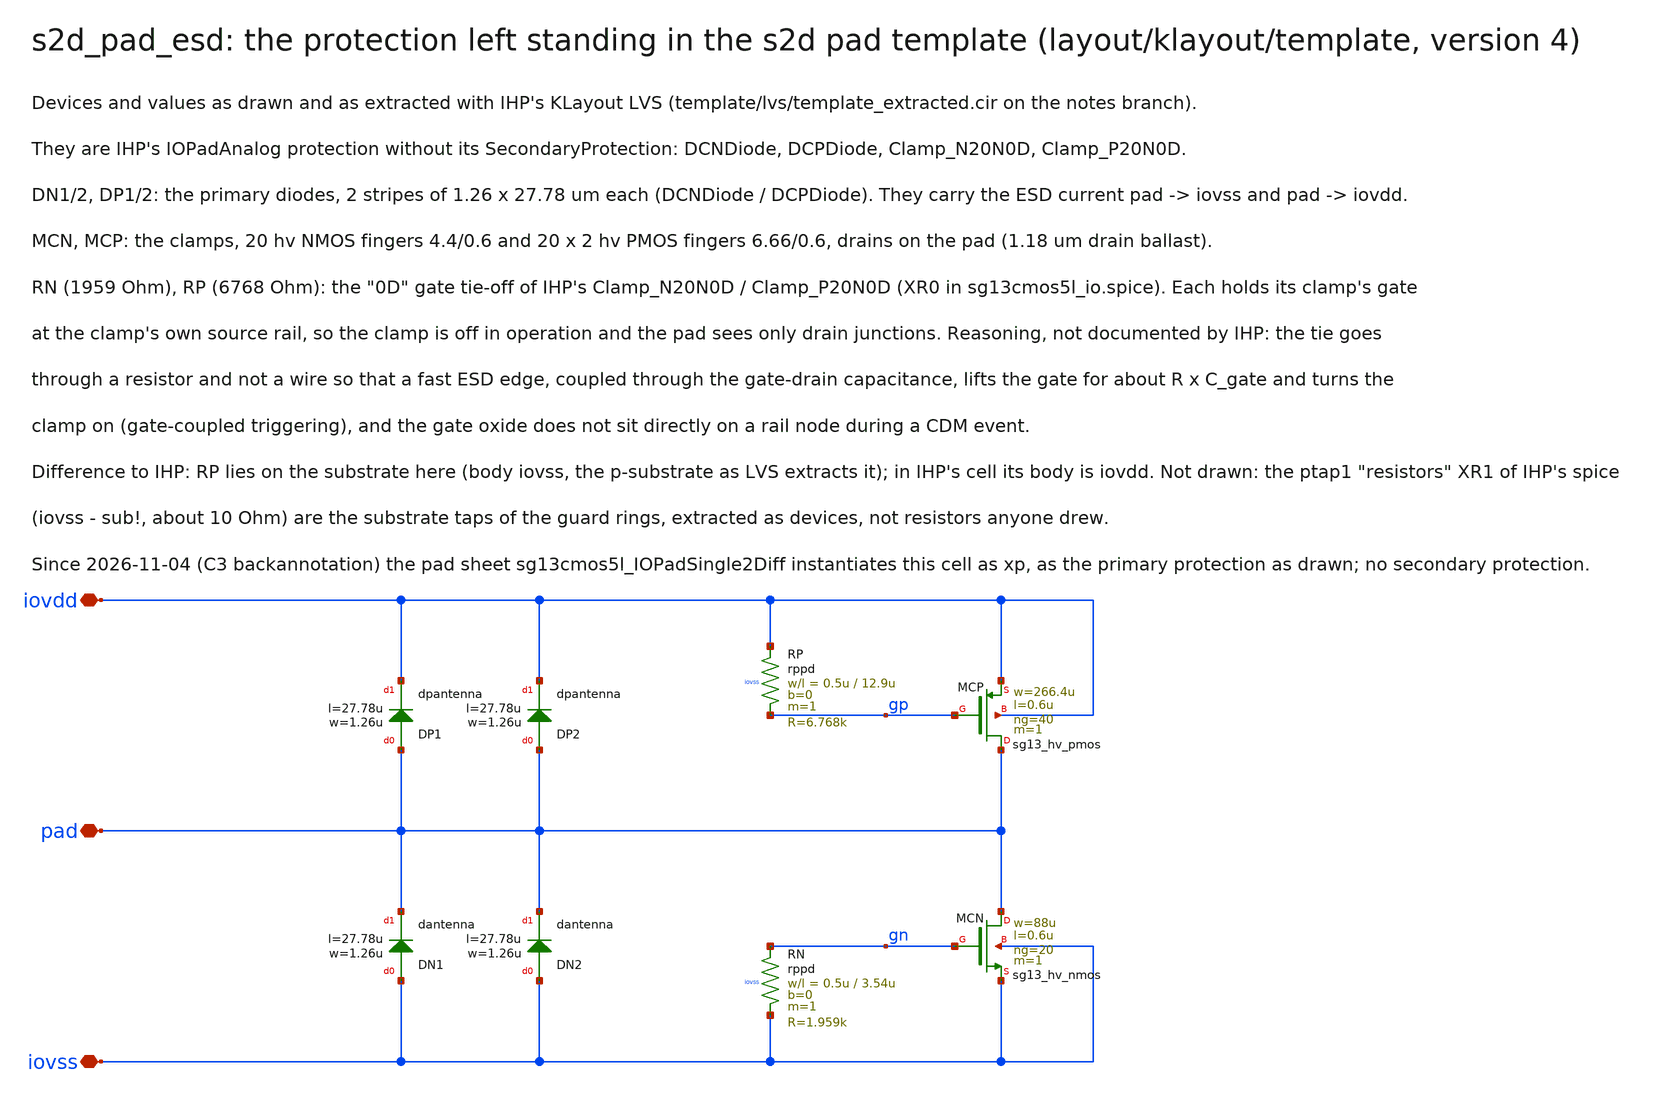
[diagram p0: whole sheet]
** sch_path: macros/sg13cmos5l_IOPadSingle2Diff/schematic/xschem/s2d_pad_esd.sch
**.subckt s2d_pad_esd iovdd iovss pad
*.iopin iovdd
*.iopin iovss
*.iopin pad
XDP1 pad iovdd dpantenna l=27.78u w=1.26u
XDN1 iovss pad dantenna l=27.78u w=1.26u
XDP2 pad iovdd dpantenna l=27.78u w=1.26u
XDN2 iovss pad dantenna l=27.78u w=1.26u
XRP iovdd gp iovss rppd w=0.5u l=12.9u m=1 b=0 mm_ok=1
XMCP pad gp iovdd iovdd sg13_hv_pmos w=266.4u l=0.6u ng=40 m=1 mm_ok=1
XRN gn iovss iovss rppd w=0.5u l=3.54u m=1 b=0 mm_ok=1
XMCN pad gn iovss iovss sg13_hv_nmos w=88u l=0.6u ng=20 m=1 mm_ok=1
**.ends
.end
